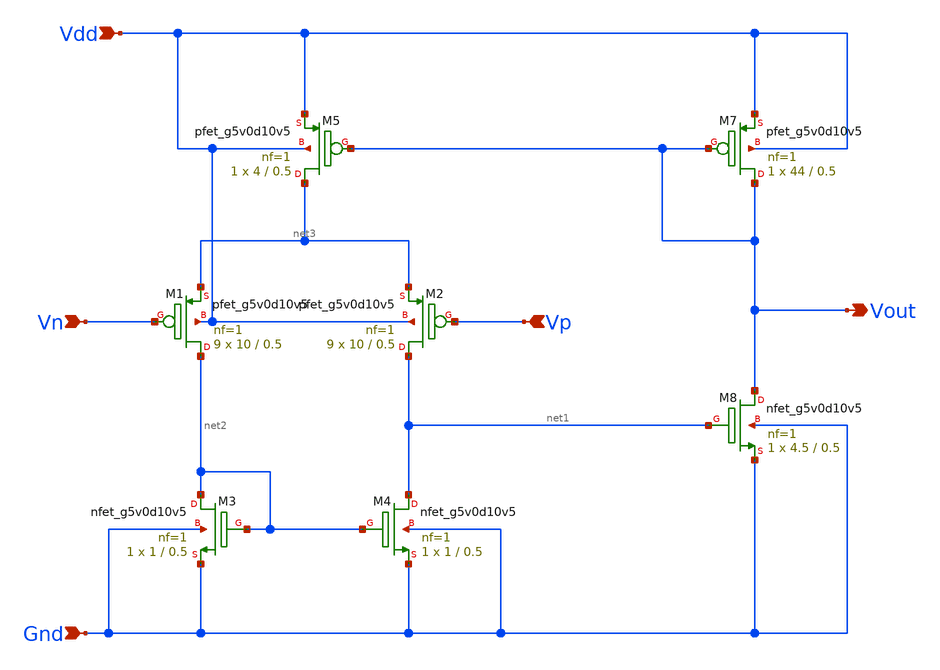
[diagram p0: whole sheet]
** sch_path: Analog_Blocks/Bandgap/Schematics/BGR1.8v_2/Bandgap1.8v_2_OTA.sch
**.subckt Bandgap1.8v_2_OTA Vdd Gnd Vp Vn Vout
*.ipin Vdd
*.ipin Gnd
*.ipin Vp
*.ipin Vn
*.opin Vout
XM5 net3 Vout Vdd Vdd sky130_fd_pr__pfet_g5v0d10v5 L=0.5 W=4 nf=1 ad='int((nf+1)/2) * W/nf * 0.29' as='int((nf+2)/2) * W/nf * 0.29'
+ pd='2*int((nf+1)/2) * (W/nf + 0.29)' ps='2*int((nf+2)/2) * (W/nf + 0.29)' nrd='0.29 / W' nrs='0.29 / W'
+ sa=0 sb=0 sd=0 mult=1 m=1
XM1 net2 Vn net3 Vdd sky130_fd_pr__pfet_g5v0d10v5 L=0.5 W=10 nf=1 ad='int((nf+1)/2) * W/nf * 0.29' as='int((nf+2)/2) * W/nf * 0.29'
+ pd='2*int((nf+1)/2) * (W/nf + 0.29)' ps='2*int((nf+2)/2) * (W/nf + 0.29)' nrd='0.29 / W' nrs='0.29 / W'
+ sa=0 sb=0 sd=0 mult=9 m=9
XM8 Vout net1 Gnd Gnd sky130_fd_pr__nfet_g5v0d10v5 L=0.5 W=4.5 nf=1 ad='int((nf+1)/2) * W/nf * 0.29'
+ as='int((nf+2)/2) * W/nf * 0.29' pd='2*int((nf+1)/2) * (W/nf + 0.29)' ps='2*int((nf+2)/2) * (W/nf + 0.29)'
+ nrd='0.29 / W' nrs='0.29 / W' sa=0 sb=0 sd=0 mult=1 m=1
XM4 net1 net2 Gnd Gnd sky130_fd_pr__nfet_g5v0d10v5 L=0.5 W=1 nf=1 ad='int((nf+1)/2) * W/nf * 0.29' as='int((nf+2)/2) * W/nf * 0.29'
+ pd='2*int((nf+1)/2) * (W/nf + 0.29)' ps='2*int((nf+2)/2) * (W/nf + 0.29)' nrd='0.29 / W' nrs='0.29 / W'
+ sa=0 sb=0 sd=0 mult=1 m=1
XM3 net2 net2 Gnd Gnd sky130_fd_pr__nfet_g5v0d10v5 L=0.5 W=1 nf=1 ad='int((nf+1)/2) * W/nf * 0.29' as='int((nf+2)/2) * W/nf * 0.29'
+ pd='2*int((nf+1)/2) * (W/nf + 0.29)' ps='2*int((nf+2)/2) * (W/nf + 0.29)' nrd='0.29 / W' nrs='0.29 / W'
+ sa=0 sb=0 sd=0 mult=1 m=1
XM2 net1 Vp net3 Vdd sky130_fd_pr__pfet_g5v0d10v5 L=0.5 W=10 nf=1 ad='int((nf+1)/2) * W/nf * 0.29' as='int((nf+2)/2) * W/nf * 0.29'
+ pd='2*int((nf+1)/2) * (W/nf + 0.29)' ps='2*int((nf+2)/2) * (W/nf + 0.29)' nrd='0.29 / W' nrs='0.29 / W'
+ sa=0 sb=0 sd=0 mult=9 m=9
XM7 Vout Vout Vdd Vdd sky130_fd_pr__pfet_g5v0d10v5 L=0.5 W=44 nf=1 ad='int((nf+1)/2) * W/nf * 0.29' as='int((nf+2)/2) * W/nf * 0.29'
+ pd='2*int((nf+1)/2) * (W/nf + 0.29)' ps='2*int((nf+2)/2) * (W/nf + 0.29)' nrd='0.29 / W' nrs='0.29 / W'
+ sa=0 sb=0 sd=0 mult=1 m=1
**.ends
.end
